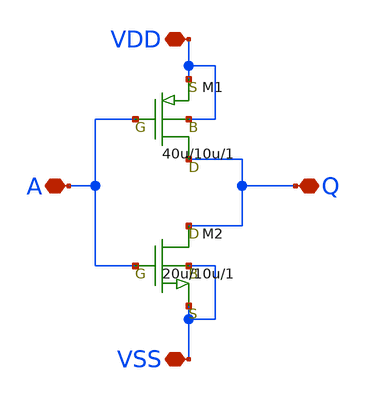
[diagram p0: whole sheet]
** sch_path: Submitted/inverter_Takuzan.sch
**.subckt inverter_Takuzan A VDD Q VSS
*.iopin A
*.iopin VDD
*.iopin Q
*.iopin VSS
M1 Q A VDD VDD pch w=40u l=10u as=0 ps=0 ad=0 pd=0 m=1
M2 Q A VSS VSS nch w=20u l=10u as=0 ps=0 ad=0 pd=0 m=1
**.ends
.end
